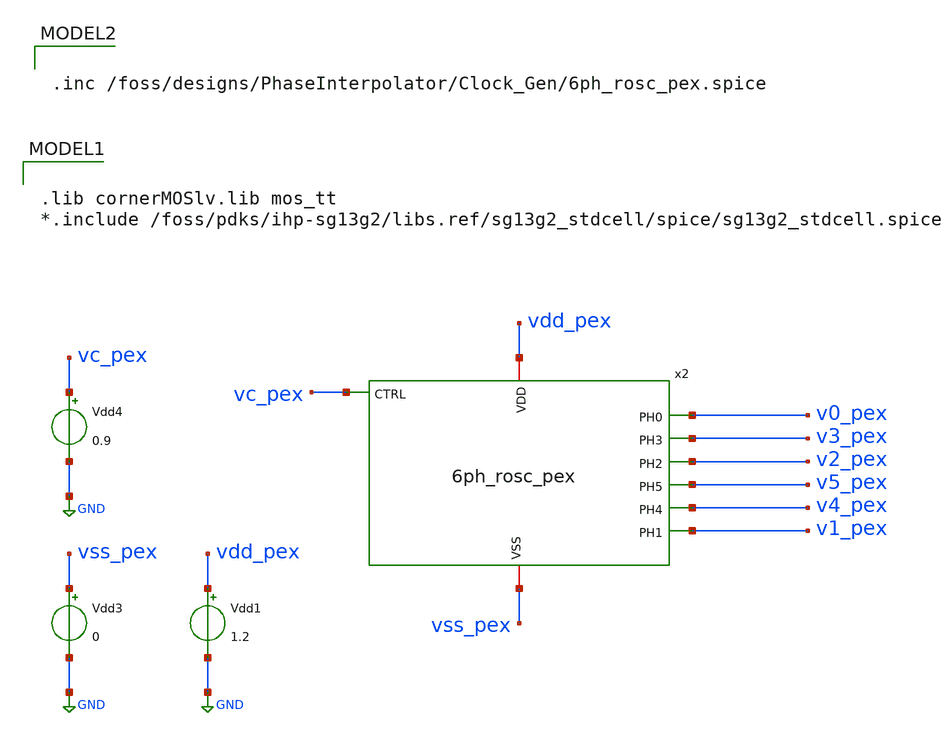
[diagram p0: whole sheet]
** sch_path: verification/testbenches/tb_6ph_rosc_pex.sch
**.subckt tb_6ph_rosc_pex
Vdd4 vc_pex GND 0.9
Vdd3 vss_pex GND 0
Vdd1 vdd_pex GND 1.2
x2 vc_pex v0_pex v3_pex v2_pex v5_pex v4_pex v1_pex vss_pex vdd_pex 6ph_rosc_pex
**** begin user architecture code

.lib cornerMOSlv.lib mos_tt
*.include /foss/pdks/ihp-sg13g2/libs.ref/sg13g2_stdcell/spice/sg13g2_stdcell.spice



.inc /foss/designs/PhaseInterpolator/Clock_Gen/6ph_rosc_pex.spice



.options rshunt = 1e12
.save v(v0) v(v1) v(v2) v(v3) v(v4) v(v5) v(v6) v(v0_pex) v(v1_pex) v(v2_pex) v(v3_pex) v(v4_pex) v(v5_pex) v(v6_pex)
.tran 2p 20n

.control
run
set color0=white
set filetype = ascii
write 6ph_rosc_pex.raw

*let period_0 = T0
*let period_1 = T1
*let period_2 = T2


meas tran T0 TRIG v(v0) VAL=0.6 RISE=5 TARG v(v0) VAL=0.6 RISE=6
meas tran T0_pex TRIG v(v0_pex) VAL=0.6 RISE=5 TARG v(v0_pex) VAL=0.6 RISE=6

let freq_0 = 1/T0
let freq_0_pex = 1/T0_pex

plot freq_0 freq_0_pex

.endc


**** end user architecture code
**.ends
.GLOBAL GND
.end
